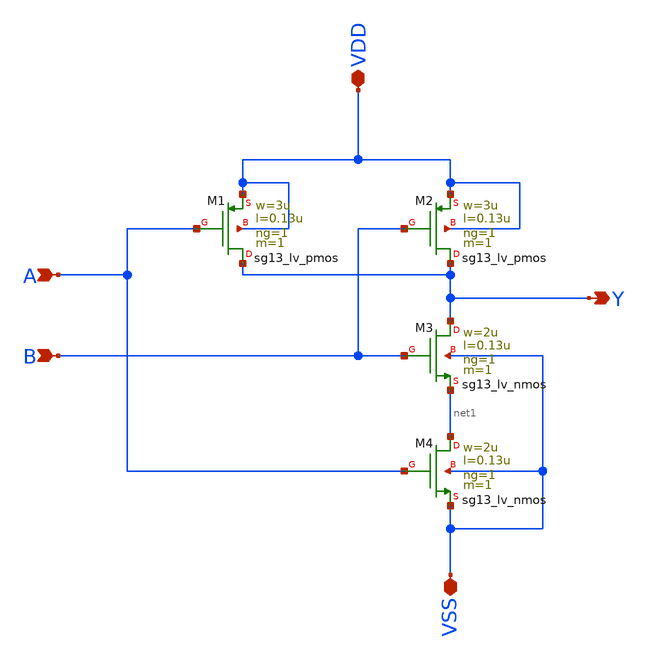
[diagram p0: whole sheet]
** sch_path: Team 1 Design/design_data/xschem/2_Input_NAND_New/New_2NAND.sch
**.subckt New_2NAND B Y A VDD VSS
*.ipin B
*.opin Y
*.ipin A
*.iopin VDD
*.iopin VSS
XM1 Y A VDD VDD sg13_lv_pmos w=3u l=0.13u ng=1 m=1 mm_ok=1
XM2 Y B VDD VDD sg13_lv_pmos w=3u l=0.13u ng=1 m=1 mm_ok=1
XM3 Y B net1 VSS sg13_lv_nmos w=2u l=0.13u ng=1 m=1 mm_ok=1
XM4 net1 A VSS VSS sg13_lv_nmos w=2u l=0.13u ng=1 m=1 mm_ok=1
**.ends
.end
